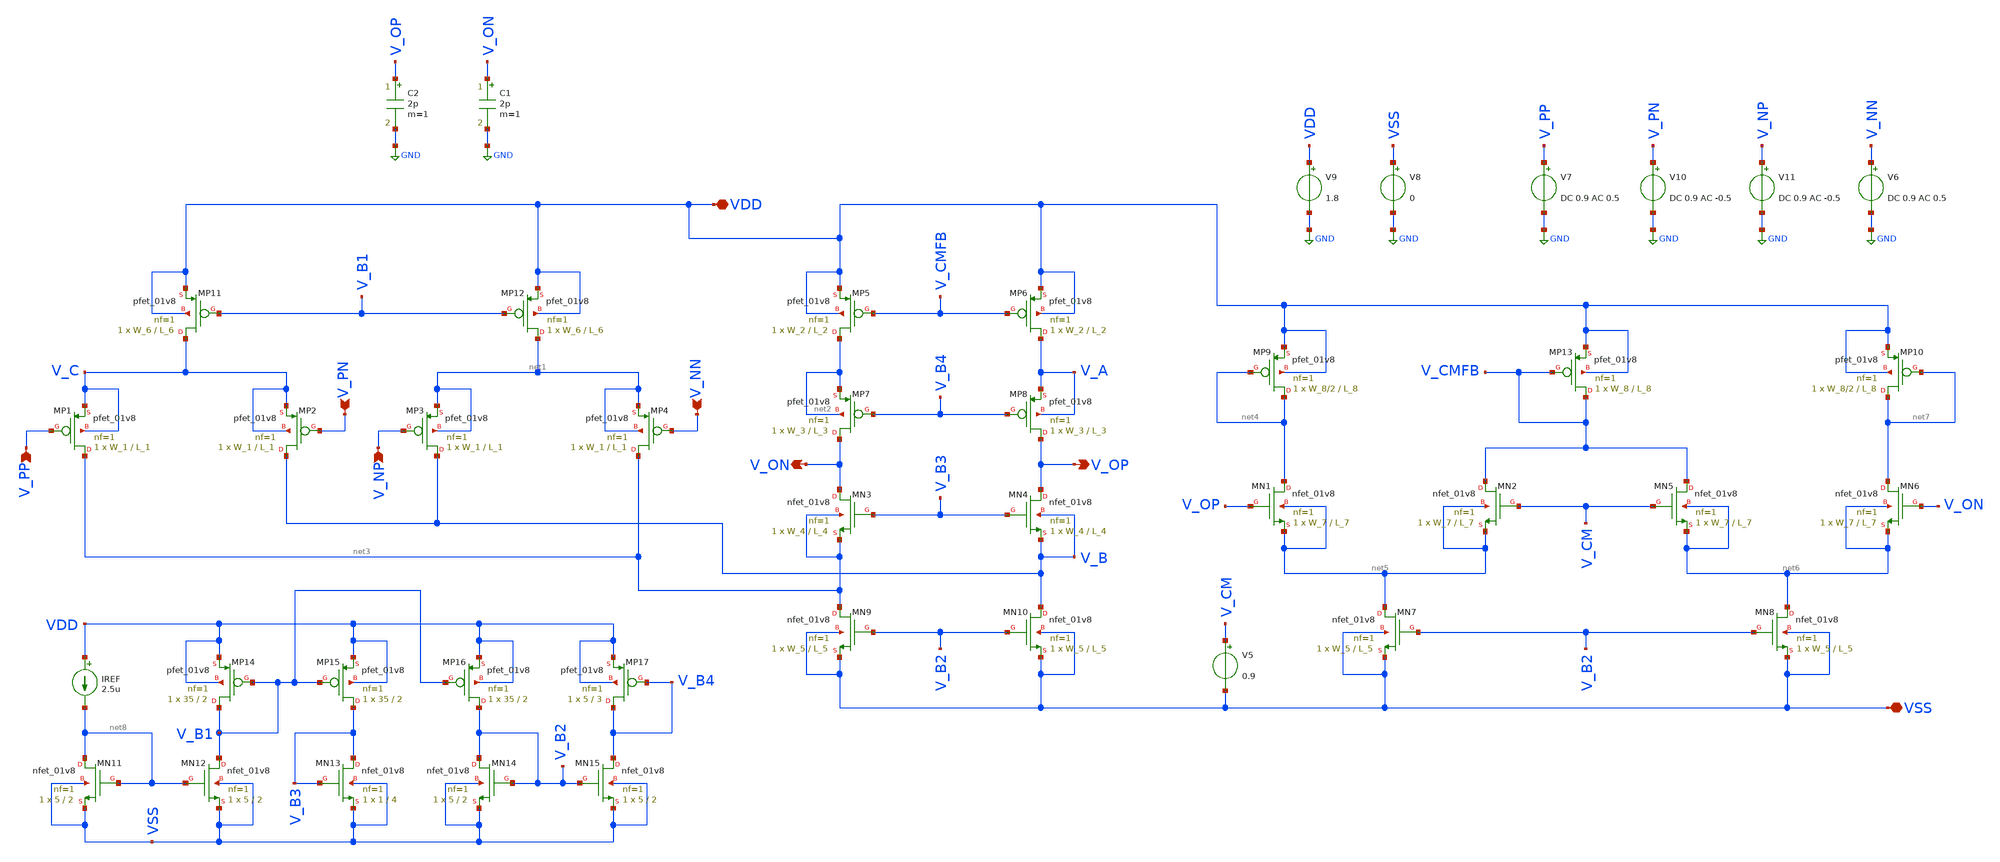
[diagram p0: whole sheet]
** sch_path: Xschem Simulations/FDDA_CMFB/tb_FDDA_CMFB_BIAS_ac.sch
**.subckt tb_FDDA_CMFB_BIAS_ac V_PP V_PN V_NP V_NN VDD V_OP V_ON VSS
*.ipin V_PP
*.ipin V_PN
*.ipin V_NP
*.ipin V_NN
*.iopin VDD
*.opin V_OP
*.opin V_ON
*.iopin VSS
XMP1 net3 V_PP V_C V_C sky130_fd_pr__pfet_01v8 L=L_1 W=W_1 nf=1 ad='int((1 + 1)/2) * W_1 / 1 * 0.29'
+ as='int((1 + 2)/2) * W_1 / 1 * 0.29' pd='2*int((1 + 1)/2) * (W_1 / 1 + 0.29)' ps='2*int((1 + 2)/2) * (W_1 / 1 + 0.29)'
+ nrd='0.29 / W_1 ' nrs='0.29 / W_1 ' sa=0 sb=0 sd=0 mult=1 m=1
XMP2 V_B V_PN V_C V_C sky130_fd_pr__pfet_01v8 L=L_1 W=W_1 nf=1 ad='int((1 + 1)/2) * W_1 / 1 * 0.29' as='int((1 + 2)/2) * W_1 / 1 * 0.29'
+ pd='2*int((1 + 1)/2) * (W_1 / 1 + 0.29)' ps='2*int((1 + 2)/2) * (W_1 / 1 + 0.29)' nrd='0.29 / W_1 ' nrs='0.29 / W_1 '
+ sa=0 sb=0 sd=0 mult=1 m=1
XMP3 V_B V_NP net1 net1 sky130_fd_pr__pfet_01v8 L=L_1 W=W_1 nf=1 ad='int((1 + 1)/2) * W_1 / 1 * 0.29'
+ as='int((1 + 2)/2) * W_1 / 1 * 0.29' pd='2*int((1 + 1)/2) * (W_1 / 1 + 0.29)' ps='2*int((1 + 2)/2) * (W_1 / 1 + 0.29)'
+ nrd='0.29 / W_1 ' nrs='0.29 / W_1 ' sa=0 sb=0 sd=0 mult=1 m=1
XMP4 net3 V_NN net1 net1 sky130_fd_pr__pfet_01v8 L=L_1 W=W_1 nf=1 ad='int((1 + 1)/2) * W_1 / 1 * 0.29'
+ as='int((1 + 2)/2) * W_1 / 1 * 0.29' pd='2*int((1 + 1)/2) * (W_1 / 1 + 0.29)' ps='2*int((1 + 2)/2) * (W_1 / 1 + 0.29)'
+ nrd='0.29 / W_1 ' nrs='0.29 / W_1 ' sa=0 sb=0 sd=0 mult=1 m=1
XMP5 net2 V_CMFB VDD VDD sky130_fd_pr__pfet_01v8 L=L_2 W=W_2 nf=1 ad='int((1 + 1)/2) * W_2 / 1 * 0.29'
+ as='int((1 + 2)/2) * W_2 / 1 * 0.29' pd='2*int((1 + 1)/2) * (W_2 / 1 + 0.29)' ps='2*int((1 + 2)/2) * (W_2 / 1 + 0.29)'
+ nrd='0.29 / W_2 ' nrs='0.29 / W_2 ' sa=0 sb=0 sd=0 mult=1 m=1
XMP6 V_A V_CMFB VDD VDD sky130_fd_pr__pfet_01v8 L=L_2 W=W_2 nf=1 ad='int((1 + 1)/2) * W_2 / 1 * 0.29'
+ as='int((1 + 2)/2) * W_2 / 1 * 0.29' pd='2*int((1 + 1)/2) * (W_2 / 1 + 0.29)' ps='2*int((1 + 2)/2) * (W_2 / 1 + 0.29)'
+ nrd='0.29 / W_2 ' nrs='0.29 / W_2 ' sa=0 sb=0 sd=0 mult=1 m=1
XMP7 V_ON V_B4 net2 net2 sky130_fd_pr__pfet_01v8 L=L_3 W=W_3 nf=1 ad='int((1 + 1)/2) * W_3 / 1 * 0.29'
+ as='int((1 + 2)/2) * W_3 / 1 * 0.29' pd='2*int((1 + 1)/2) * (W_3 / 1 + 0.29)' ps='2*int((1 + 2)/2) * (W_3 / 1 + 0.29)'
+ nrd='0.29 / W_3 ' nrs='0.29 / W_3 ' sa=0 sb=0 sd=0 mult=1 m=1
XMP8 V_OP V_B4 V_A V_A sky130_fd_pr__pfet_01v8 L=L_3 W=W_3 nf=1 ad='int((1 + 1)/2) * W_3 / 1 * 0.29'
+ as='int((1 + 2)/2) * W_3 / 1 * 0.29' pd='2*int((1 + 1)/2) * (W_3 / 1 + 0.29)' ps='2*int((1 + 2)/2) * (W_3 / 1 + 0.29)'
+ nrd='0.29 / W_3 ' nrs='0.29 / W_3 ' sa=0 sb=0 sd=0 mult=1 m=1
XMP11 V_C V_B1 VDD VDD sky130_fd_pr__pfet_01v8 L=L_6 W=W_6 nf=1 ad='int((1 + 1)/2) * W_6 / 1 * 0.29'
+ as='int((1 + 2)/2) * W_6 / 1 * 0.29' pd='2*int((1 + 1)/2) * (W_6 / 1 + 0.29)' ps='2*int((1 + 2)/2) * (W_6 / 1 + 0.29)'
+ nrd='0.29 / W_6 ' nrs='0.29 / W_6 ' sa=0 sb=0 sd=0 mult=1 m=1
XMP12 net1 V_B1 VDD VDD sky130_fd_pr__pfet_01v8 L=L_6 W=W_6 nf=1 ad='int((1 + 1)/2) * W_6 / 1 * 0.29'
+ as='int((1 + 2)/2) * W_6 / 1 * 0.29' pd='2*int((1 + 1)/2) * (W_6 / 1 + 0.29)' ps='2*int((1 + 2)/2) * (W_6 / 1 + 0.29)'
+ nrd='0.29 / W_6 ' nrs='0.29 / W_6 ' sa=0 sb=0 sd=0 mult=1 m=1
XMN3 V_ON V_B3 net3 net3 sky130_fd_pr__nfet_01v8 L=L_4 W=W_4 nf=1 ad='int((1 + 1)/2) * W_4 / 1 * 0.29'
+ as='int((1 + 2)/2) * W_4 / 1 * 0.29' pd='2*int((1 + 1)/2) * (W_4 / 1 + 0.29)' ps='2*int((1 + 2)/2) * (W_4 / 1 + 0.29)'
+ nrd='0.29 / W_4 ' nrs='0.29 / W_4 ' sa=0 sb=0 sd=0 mult=1 m=1
XMN4 V_OP V_B3 V_B V_B sky130_fd_pr__nfet_01v8 L=L_4 W=W_4 nf=1 ad='int((1 + 1)/2) * W_4 / 1 * 0.29'
+ as='int((1 + 2)/2) * W_4 / 1 * 0.29' pd='2*int((1 + 1)/2) * (W_4 / 1 + 0.29)' ps='2*int((1 + 2)/2) * (W_4 / 1 + 0.29)'
+ nrd='0.29 / W_4 ' nrs='0.29 / W_4 ' sa=0 sb=0 sd=0 mult=1 m=1
XMN9 net3 V_B2 VSS VSS sky130_fd_pr__nfet_01v8 L=L_5 W=W_5 nf=1 ad='int((1 + 1)/2) * W_5 / 1 * 0.29'
+ as='int((1 + 2)/2) * W_5 / 1 * 0.29' pd='2*int((1 + 1)/2) * (W_5 / 1 + 0.29)' ps='2*int((1 + 2)/2) * (W_5 / 1 + 0.29)'
+ nrd='0.29 / W_5 ' nrs='0.29 / W_5 ' sa=0 sb=0 sd=0 mult=1 m=1
XMN10 V_B V_B2 VSS VSS sky130_fd_pr__nfet_01v8 L=L_5 W=W_5 nf=1 ad='int((1 + 1)/2) * W_5 / 1 * 0.29'
+ as='int((1 + 2)/2) * W_5 / 1 * 0.29' pd='2*int((1 + 1)/2) * (W_5 / 1 + 0.29)' ps='2*int((1 + 2)/2) * (W_5 / 1 + 0.29)'
+ nrd='0.29 / W_5 ' nrs='0.29 / W_5 ' sa=0 sb=0 sd=0 mult=1 m=1
XMN1 net4 V_OP net5 net5 sky130_fd_pr__nfet_01v8 L=L_7 W=W_7 nf=1 ad='int((1 + 1)/2) * W_7 / 1 * 0.29'
+ as='int((1 + 2)/2) * W_7 / 1 * 0.29' pd='2*int((1 + 1)/2) * (W_7 / 1 + 0.29)' ps='2*int((1 + 2)/2) * (W_7 / 1 + 0.29)'
+ nrd='0.29 / W_7 ' nrs='0.29 / W_7 ' sa=0 sb=0 sd=0 mult=1 m=1
XMN2 V_CMFB V_CM net5 net5 sky130_fd_pr__nfet_01v8 L=L_7 W=W_7 nf=1 ad='int((1 + 1)/2) * W_7 / 1 * 0.29'
+ as='int((1 + 2)/2) * W_7 / 1 * 0.29' pd='2*int((1 + 1)/2) * (W_7 / 1 + 0.29)' ps='2*int((1 + 2)/2) * (W_7 / 1 + 0.29)'
+ nrd='0.29 / W_7 ' nrs='0.29 / W_7 ' sa=0 sb=0 sd=0 mult=1 m=1
XMN7 net5 V_B2 VSS VSS sky130_fd_pr__nfet_01v8 L=L_5 W=W_5 nf=1 ad='int((1 + 1)/2) * W_5 / 1 * 0.29'
+ as='int((1 + 2)/2) * W_5 / 1 * 0.29' pd='2*int((1 + 1)/2) * (W_5 / 1 + 0.29)' ps='2*int((1 + 2)/2) * (W_5 / 1 + 0.29)'
+ nrd='0.29 / W_5 ' nrs='0.29 / W_5 ' sa=0 sb=0 sd=0 mult=1 m=1
XMN6 net7 V_ON net6 net6 sky130_fd_pr__nfet_01v8 L=L_7 W=W_7 nf=1 ad='int((1 + 1)/2) * W_7 / 1 * 0.29'
+ as='int((1 + 2)/2) * W_7 / 1 * 0.29' pd='2*int((1 + 1)/2) * (W_7 / 1 + 0.29)' ps='2*int((1 + 2)/2) * (W_7 / 1 + 0.29)'
+ nrd='0.29 / W_7 ' nrs='0.29 / W_7 ' sa=0 sb=0 sd=0 mult=1 m=1
XMN5 V_CMFB V_CM net6 net6 sky130_fd_pr__nfet_01v8 L=L_7 W=W_7 nf=1 ad='int((1 + 1)/2) * W_7 / 1 * 0.29'
+ as='int((1 + 2)/2) * W_7 / 1 * 0.29' pd='2*int((1 + 1)/2) * (W_7 / 1 + 0.29)' ps='2*int((1 + 2)/2) * (W_7 / 1 + 0.29)'
+ nrd='0.29 / W_7 ' nrs='0.29 / W_7 ' sa=0 sb=0 sd=0 mult=1 m=1
XMN8 net6 V_B2 VSS VSS sky130_fd_pr__nfet_01v8 L=L_5 W=W_5 nf=1 ad='int((1 + 1)/2) * W_5 / 1 * 0.29'
+ as='int((1 + 2)/2) * W_5 / 1 * 0.29' pd='2*int((1 + 1)/2) * (W_5 / 1 + 0.29)' ps='2*int((1 + 2)/2) * (W_5 / 1 + 0.29)'
+ nrd='0.29 / W_5 ' nrs='0.29 / W_5 ' sa=0 sb=0 sd=0 mult=1 m=1
XMP9 net4 net4 VDD VDD sky130_fd_pr__pfet_01v8 L=L_8 W=W_8/2 nf=1 ad='int((1 + 1)/2) * W_8/2 / 1 * 0.29'
+ as='int((1 + 2)/2) * W_8/2 / 1 * 0.29' pd='2*int((1 + 1)/2) * (W_8/2 / 1 + 0.29)' ps='2*int((1 + 2)/2) * (W_8/2 / 1 + 0.29)'
+ nrd='0.29 / W_8/2 ' nrs='0.29 / W_8/2 ' sa=0 sb=0 sd=0 mult=1 m=1
XMP13 V_CMFB V_CMFB VDD VDD sky130_fd_pr__pfet_01v8 L=L_8 W=W_8 nf=1 ad='int((1 + 1)/2) * W_8 / 1 * 0.29'
+ as='int((1 + 2)/2) * W_8 / 1 * 0.29' pd='2*int((1 + 1)/2) * (W_8 / 1 + 0.29)' ps='2*int((1 + 2)/2) * (W_8 / 1 + 0.29)'
+ nrd='0.29 / W_8 ' nrs='0.29 / W_8 ' sa=0 sb=0 sd=0 mult=1 m=1
XMP10 net7 net7 VDD VDD sky130_fd_pr__pfet_01v8 L=L_8 W=W_8/2 nf=1 ad='int((1 + 1)/2) * W_8/2 / 1 * 0.29'
+ as='int((1 + 2)/2) * W_8/2 / 1 * 0.29' pd='2*int((1 + 1)/2) * (W_8/2 / 1 + 0.29)' ps='2*int((1 + 2)/2) * (W_8/2 / 1 + 0.29)'
+ nrd='0.29 / W_8/2 ' nrs='0.29 / W_8/2 ' sa=0 sb=0 sd=0 mult=1 m=1
V5 V_CM VSS 0.9
V10 V_PN GND DC 0.9 AC -0.5
V7 V_PP GND DC 0.9 AC 0.5
V8 VSS GND 0
V9 VDD GND 1.8
V6 V_NN GND DC 0.9 AC 0.5
V11 V_NP GND DC 0.9 AC -0.5
C1 V_ON GND 2p m=1
C2 V_OP GND 2p m=1
XMN11 net8 net8 VSS VSS sky130_fd_pr__nfet_01v8 L=2 W=5 nf=1 ad='int((1 + 1)/2) * 5 / 1 * 0.29' as='int((1 + 2)/2) * 5 / 1 * 0.29'
+ pd='2*int((1 + 1)/2) * (5 / 1 + 0.29)' ps='2*int((1 + 2)/2) * (5 / 1 + 0.29)' nrd='0.29 / 5 ' nrs='0.29 / 5 '
+ sa=0 sb=0 sd=0 mult=1 m=1
XMP14 V_B1 V_B1 VDD VDD sky130_fd_pr__pfet_01v8 L=2 W=35 nf=1 ad='int((1 + 1)/2) * 35 / 1 * 0.29' as='int((1 + 2)/2) * 35 / 1 * 0.29'
+ pd='2*int((1 + 1)/2) * (35 / 1 + 0.29)' ps='2*int((1 + 2)/2) * (35 / 1 + 0.29)' nrd='0.29 / 35 ' nrs='0.29 / 35 '
+ sa=0 sb=0 sd=0 mult=1 m=1
IREF VDD net8 2.5u
XMN12 V_B1 net8 VSS VSS sky130_fd_pr__nfet_01v8 L=2 W=5 nf=1 ad='int((1 + 1)/2) * 5 / 1 * 0.29' as='int((1 + 2)/2) * 5 / 1 * 0.29'
+ pd='2*int((1 + 1)/2) * (5 / 1 + 0.29)' ps='2*int((1 + 2)/2) * (5 / 1 + 0.29)' nrd='0.29 / 5 ' nrs='0.29 / 5 '
+ sa=0 sb=0 sd=0 mult=1 m=1
XMP15 V_B3 V_B1 VDD VDD sky130_fd_pr__pfet_01v8 L=2 W=35 nf=1 ad='int((1 + 1)/2) * 35 / 1 * 0.29' as='int((1 + 2)/2) * 35 / 1 * 0.29'
+ pd='2*int((1 + 1)/2) * (35 / 1 + 0.29)' ps='2*int((1 + 2)/2) * (35 / 1 + 0.29)' nrd='0.29 / 35 ' nrs='0.29 / 35 '
+ sa=0 sb=0 sd=0 mult=1 m=1
XMP16 V_B2 V_B1 VDD VDD sky130_fd_pr__pfet_01v8 L=2 W=35 nf=1 ad='int((1 + 1)/2) * 35 / 1 * 0.29' as='int((1 + 2)/2) * 35 / 1 * 0.29'
+ pd='2*int((1 + 1)/2) * (35 / 1 + 0.29)' ps='2*int((1 + 2)/2) * (35 / 1 + 0.29)' nrd='0.29 / 35 ' nrs='0.29 / 35 '
+ sa=0 sb=0 sd=0 mult=1 m=1
XMN13 V_B3 V_B3 VSS VSS sky130_fd_pr__nfet_01v8 L=4 W=1 nf=1 ad='int((1 + 1)/2) * 1 / 1 * 0.29' as='int((1 + 2)/2) * 1 / 1 * 0.29'
+ pd='2*int((1 + 1)/2) * (1 / 1 + 0.29)' ps='2*int((1 + 2)/2) * (1 / 1 + 0.29)' nrd='0.29 / 1 ' nrs='0.29 / 1 '
+ sa=0 sb=0 sd=0 mult=1 m=1
XMN14 V_B2 V_B2 VSS VSS sky130_fd_pr__nfet_01v8 L=2 W=5 nf=1 ad='int((1 + 1)/2) * 5 / 1 * 0.29' as='int((1 + 2)/2) * 5 / 1 * 0.29'
+ pd='2*int((1 + 1)/2) * (5 / 1 + 0.29)' ps='2*int((1 + 2)/2) * (5 / 1 + 0.29)' nrd='0.29 / 5 ' nrs='0.29 / 5 '
+ sa=0 sb=0 sd=0 mult=1 m=1
XMN15 V_B4 V_B2 VSS VSS sky130_fd_pr__nfet_01v8 L=2 W=5 nf=1 ad='int((1 + 1)/2) * 5 / 1 * 0.29' as='int((1 + 2)/2) * 5 / 1 * 0.29'
+ pd='2*int((1 + 1)/2) * (5 / 1 + 0.29)' ps='2*int((1 + 2)/2) * (5 / 1 + 0.29)' nrd='0.29 / 5 ' nrs='0.29 / 5 '
+ sa=0 sb=0 sd=0 mult=1 m=1
XMP17 V_B4 V_B4 VDD VDD sky130_fd_pr__pfet_01v8 L=3 W=5 nf=1 ad='int((1 + 1)/2) * 5 / 1 * 0.29' as='int((1 + 2)/2) * 5 / 1 * 0.29'
+ pd='2*int((1 + 1)/2) * (5 / 1 + 0.29)' ps='2*int((1 + 2)/2) * (5 / 1 + 0.29)' nrd='0.29 / 5 ' nrs='0.29 / 5 '
+ sa=0 sb=0 sd=0 mult=1 m=1
**** begin user architecture code

** opencircuitdesign pdks install
.lib $::SKYWATER_MODELS/sky130.lib.spice tt



.control
  save all
  ac dec 20 0.1 1G

  let vout = v(v_op) - v(v_on)
  let vin = (v(v_pp) - v(v_pn)) - (v(v_np) - v(v_nn))

  let gain = vout / vin
  let db_gain = db(gain)
  let deg_phase = 180*cph(v(vout))/pi

  meas ac gain_DC FIND db_gain AT=1

  meas ac gbw_freq WHEN db_gain=0 FALL=1
  let gbw_Mfreq = gbw_freq * 1e-6

  meas ac pm_deg FIND deg_phase AT=gbw_freq
  let pm = 180 + pm_deg

  plot db_gain deg_phase
  print gain_DC
  print gbw_Mfreq
  print pm
.endc




.param temp=25
.option savecurrents
.param W_1=88
.param W_2=88
.param W_3=88
.param W_4=14
.param W_5=28
.param W_6=176
.param W_7=14
.param W_8=176
.param L_1=1
.param L_2=1
.param L_3=1
.param L_4=1
.param L_5=1
.param L_6=1
.param L_7=1
.param L_8=1
.control
  save all
  op
  write tb_FDDA_CMFB_BIAS_ac.raw
.endc


**** end user architecture code
**.ends
.GLOBAL GND
.end
